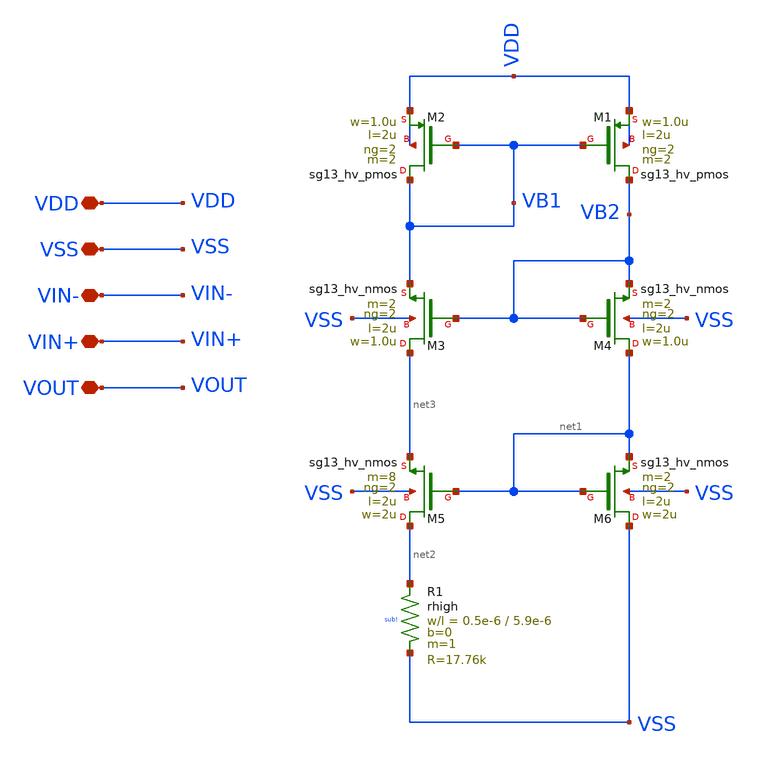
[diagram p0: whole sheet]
** sch_path: my_ip/LIB/ihp-sg13g2/VA001/VA001.sch
**.subckt VA001 VDD VSS VIN- VIN+ VOUT
*.iopin VDD
*.iopin VSS
*.iopin VIN-
*.iopin VIN+
*.iopin VOUT
XM2 VB1 VB1 VDD VDD sg13_hv_pmos w=1.0u l=2u ng=2 m=2 mm_ok=1
XM1 VB2 VB1 VDD VDD sg13_hv_pmos w=1.0u l=2u ng=2 m=2 mm_ok=1
XM3 net3 VB2 VB1 VSS sg13_hv_nmos w=1.0u l=2u ng=2 m=2 mm_ok=1
XM4 net1 VB2 VB2 VSS sg13_hv_nmos w=1.0u l=2u ng=2 m=2 mm_ok=1
XM5 net2 net1 net3 VSS sg13_hv_nmos w=2u l=2u ng=2 m=8 mm_ok=1
XM6 VSS net1 net1 VSS sg13_hv_nmos w=2u l=2u ng=2 m=2 mm_ok=1
XR1 net2 VSS sub! rhigh w=0.5e-6 l=5.9e-6 m=1 b=0 mm_ok=1
**.ends
.end
